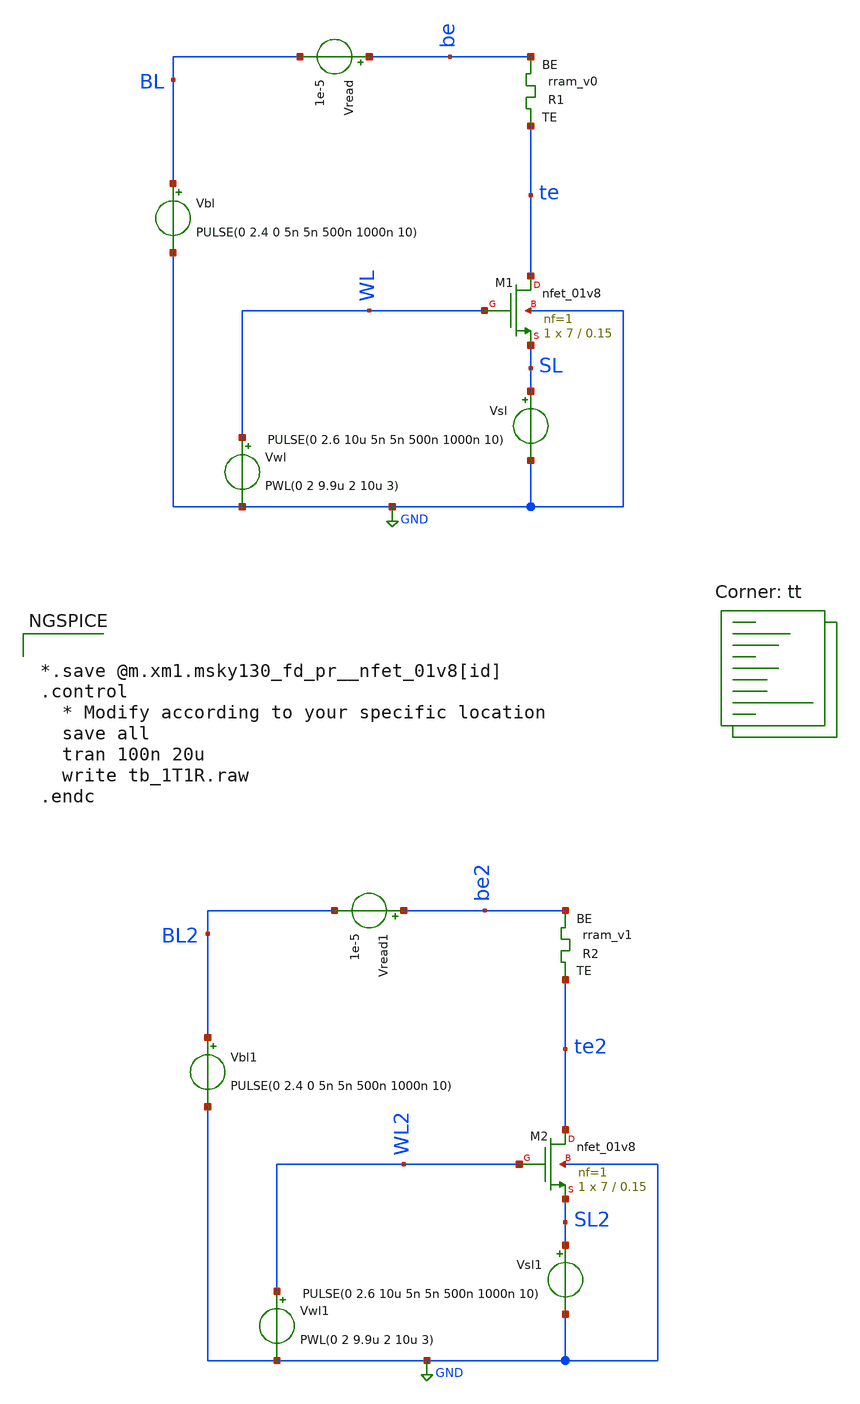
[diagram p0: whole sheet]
** sch_path: memristor_models/wellposed/tb_1T1R.sch
**.subckt tb_1T1R
XM1 te WL SL GND sky130_fd_pr__nfet_01v8 L=0.15 W=7 nf=1 ad='int((nf+1)/2) * W/nf * 0.29' as='int((nf+2)/2) * W/nf * 0.29'
+ pd='2*int((nf+1)/2) * (W/nf + 0.29)' ps='2*int((nf+2)/2) * (W/nf + 0.29)' nrd='0.29 / W' nrs='0.29 / W'
+ sa=0 sb=0 sd=0 mult=1 m=1
Vwl WL GND PWL(0 2 9.9u 2 10u 3)
Vbl BL GND PULSE(0 2.4 0 5n 5n 500n 1000n 10)
Vread be BL 1e-5
XR1 te be rram_v0
Vsl SL GND PULSE(0 2.6 10u 5n 5n 500n 1000n 10)
XM2 te2 WL2 SL2 GND sky130_fd_pr__nfet_01v8 L=0.15 W=7 nf=1 ad='int((nf+1)/2) * W/nf * 0.29' as='int((nf+2)/2) * W/nf * 0.29'
+ pd='2*int((nf+1)/2) * (W/nf + 0.29)' ps='2*int((nf+2)/2) * (W/nf + 0.29)' nrd='0.29 / W' nrs='0.29 / W'
+ sa=0 sb=0 sd=0 mult=1 m=1
Vwl1 WL2 GND PWL(0 2 9.9u 2 10u 3)
Vbl1 BL2 GND PULSE(0 2.4 0 5n 5n 500n 1000n 10)
Vread1 be2 BL2 1e-5
XR2 te2 be2 rram_v1
Vsl1 SL2 GND PULSE(0 2.6 10u 5n 5n 500n 1000n 10)
**** begin user architecture code


*.save @m.xm1.msky130_fd_pr__nfet_01v8[id]
.control
  * Modify according to your specific location
  save all
  tran 100n 20u
  write tb_1T1R.raw
.endc



.lib $::SKYWATER_MODELS/sky130.lib.spice tt

.subckt rram_v0 TE BE
	N1 TE BE rram_v0_model gap_initial=0.11
.ends rram_v0

.subckt rram_v1 TE BE
	N1 TE BE rram_v0_model gap_initial=1.68
.ends rram_v1

.model rram_v0_model rram_v0_va
.control
pre_osdi /home/alex/pdk/sky130B/libs.tech/ngspice/rram_v0.osdi
.endc

**** end user architecture code
**.ends
.GLOBAL GND
.end
